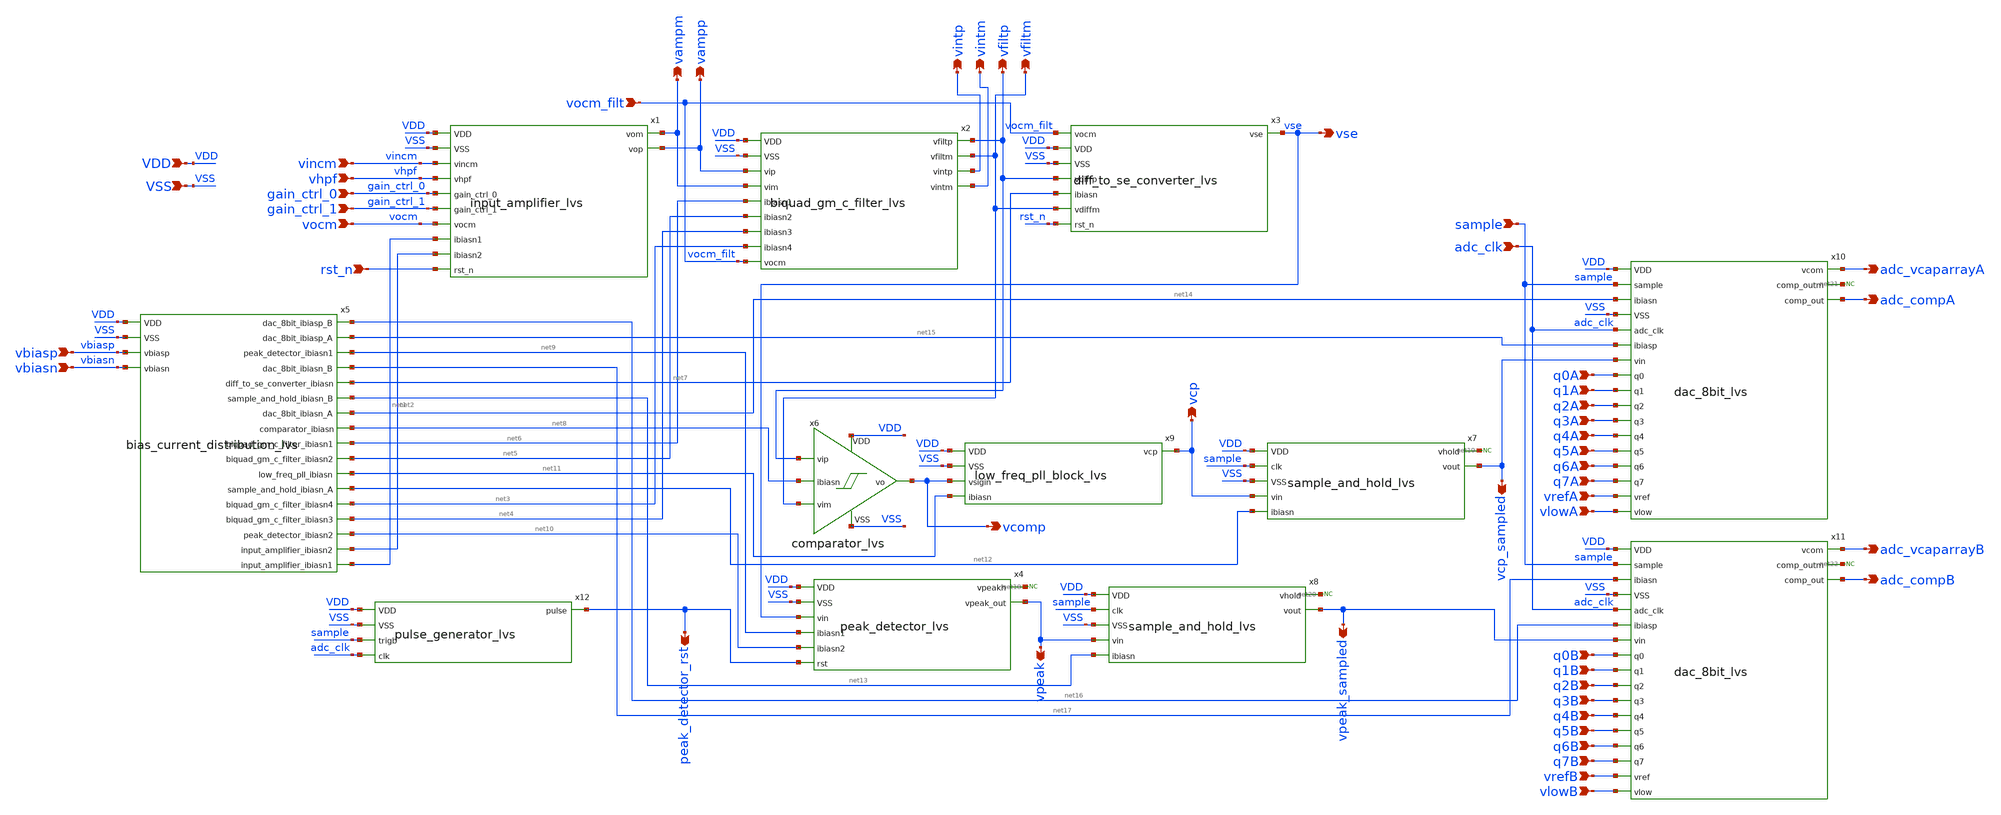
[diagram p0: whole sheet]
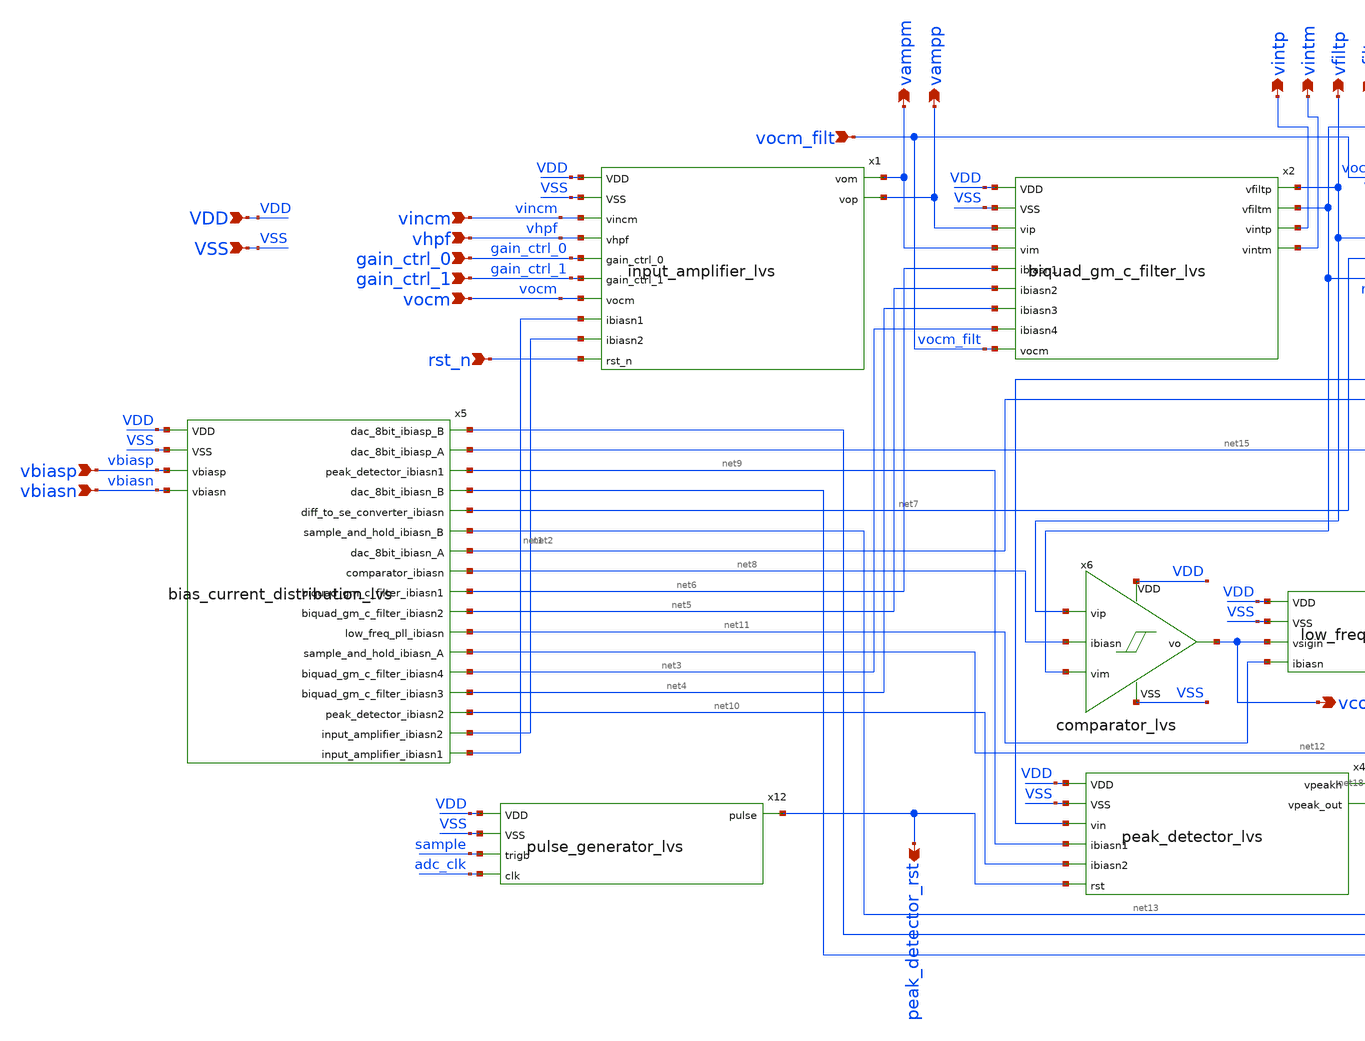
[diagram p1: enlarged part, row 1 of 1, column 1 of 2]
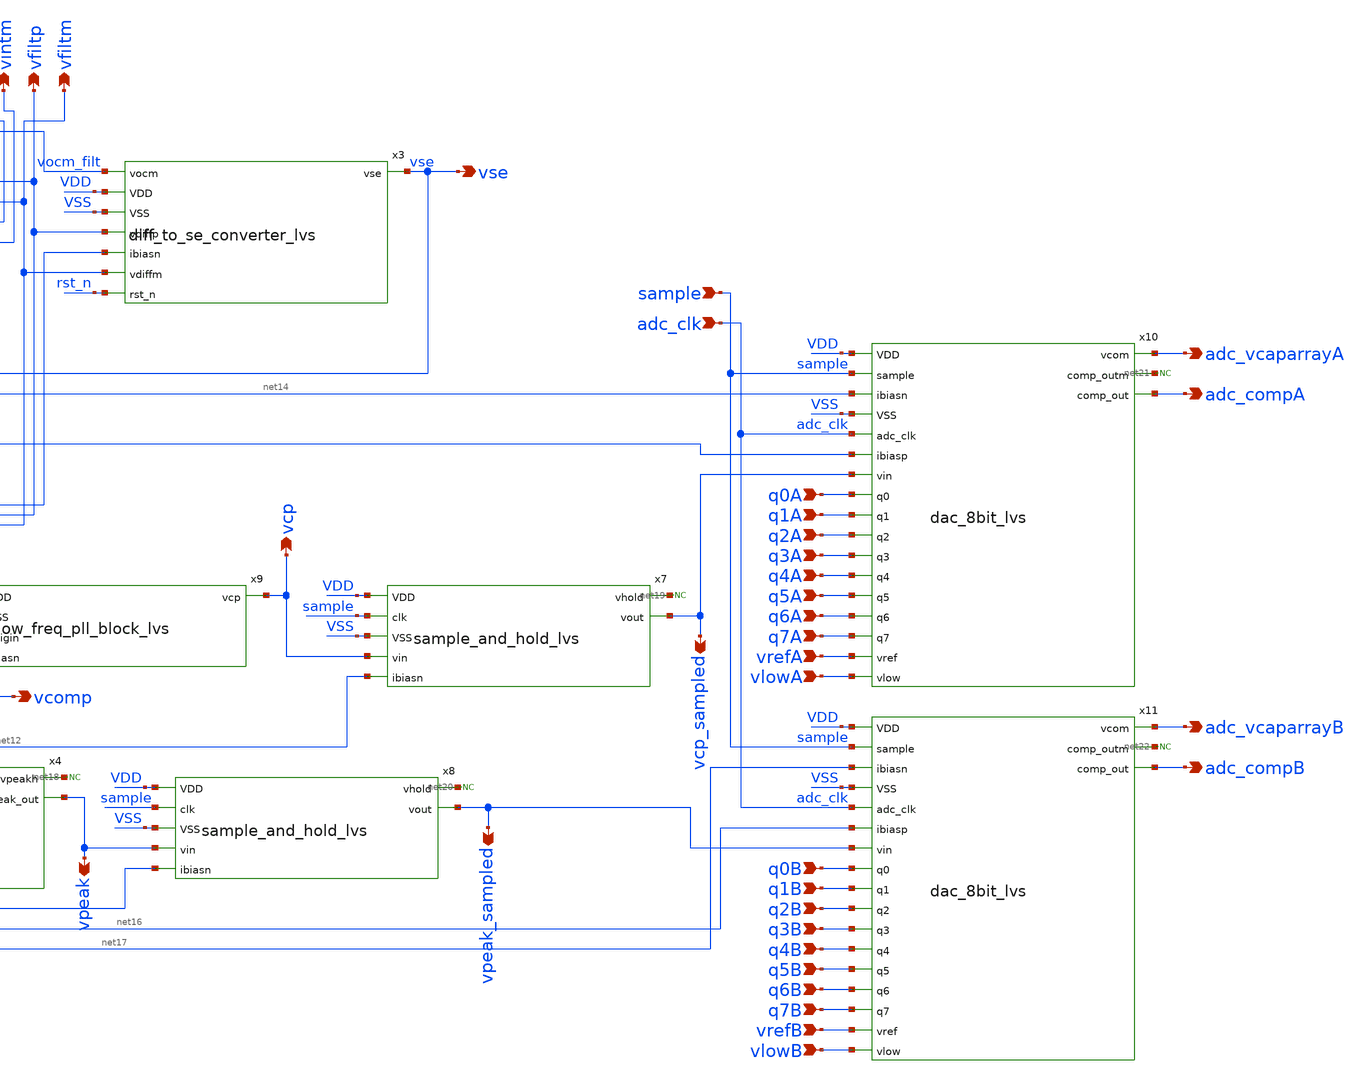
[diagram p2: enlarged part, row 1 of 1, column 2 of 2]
** sch_path: designs/analog_top_level_lvs.sch
**.subckt analog_top_level_lvs vintp vintm vfiltp vfiltm vlowA vrefA q7A q6A q5A q4A q3A q2A q1A q0A
*+ adc_clk sample vlowB vrefB q7B q6B q5B q4B q3B q2B q1B q0B adc_compA adc_compB vcp vcp_sampled
*+ vpeak_sampled vpeak vse vcomp vhpf VDD VSS vincm vocm vocm_filt gain_ctrl_0 gain_ctrl_1 vbiasp vbiasn
*+ peak_detector_rst vampm vampp adc_vcaparrayB adc_vcaparrayA rst_n
*.opin vintp
*.opin vintm
*.opin vfiltp
*.opin vfiltm
*.ipin vlowA
*.ipin vrefA
*.ipin q7A
*.ipin q6A
*.ipin q5A
*.ipin q4A
*.ipin q3A
*.ipin q2A
*.ipin q1A
*.ipin q0A
*.ipin adc_clk
*.ipin sample
*.ipin vlowB
*.ipin vrefB
*.ipin q7B
*.ipin q6B
*.ipin q5B
*.ipin q4B
*.ipin q3B
*.ipin q2B
*.ipin q1B
*.ipin q0B
*.opin adc_compA
*.opin adc_compB
*.opin vcp
*.opin vcp_sampled
*.opin vpeak_sampled
*.opin vpeak
*.opin vse
*.opin vcomp
*.ipin vhpf
*.ipin VDD
*.ipin VSS
*.ipin vincm
*.ipin vocm
*.ipin vocm_filt
*.ipin gain_ctrl_0
*.ipin gain_ctrl_1
*.ipin vbiasp
*.ipin vbiasn
*.opin peak_detector_rst
*.opin vampm
*.opin vampp
*.opin adc_vcaparrayB
*.opin adc_vcaparrayA
*.ipin rst_n
x1 VDD VSS vincm vhpf gain_ctrl_0 gain_ctrl_1 vocm net1 net2 rst_n vampm vampp input_amplifier_lvs
x2 VDD VSS vampp vampm net6 net5 net4 net3 vocm_filt vfiltp vfiltm vintp vintm
+ biquad_gm_c_filter_lvs
x3 vocm_filt VDD VSS vfiltp vse net7 vfiltm rst_n diff_to_se_converter_lvs
x5 VDD VSS net16 net15 vbiasp vbiasn net9 net17 net7 net13 net14 net8 net6 net5 net11 net12 net3
+ net4 net10 net2 net1 bias_current_distribution_lvs
x6 vfiltp vfiltm vcomp net8 VDD VSS comparator_lvs
x4 VDD VSS vse net9 net18 vpeak net10 peak_detector_rst peak_detector_lvs
* noconn #net18
x7 VDD sample VSS net19 vcp vcp_sampled net12 sample_and_hold_lvs
x8 VDD sample VSS net20 vpeak vpeak_sampled net13 sample_and_hold_lvs
x9 vcp VDD VSS vcomp net11 low_freq_pll_block_lvs
* noconn #net20
* noconn #net19
x10 adc_vcaparrayA VDD sample net14 net21 VSS adc_compA adc_clk net15 vcp_sampled q0A q1A q2A q7A
+ q3A q4A q5A q6A vrefA vlowA dac_8bit_lvs
x11 adc_vcaparrayB VDD sample net17 net22 VSS adc_compB adc_clk net16 vpeak_sampled q0B q1B q2B q7B
+ q3B q4B q5B q6B vrefB vlowB dac_8bit_lvs
* noconn #net21
* noconn #net22
x12 VDD VSS sample peak_detector_rst adc_clk pulse_generator_lvs
**.ends
.end
